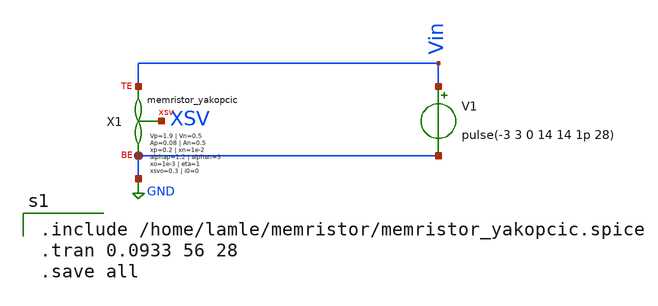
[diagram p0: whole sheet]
** sch_path: apl-paper/ngspice/test_memristor.sch
**.subckt test_memristor
V1 Vin GND pulse(-3 3 0 14 14 1p 28)
X1 GND Vin XSV memristor_yakopcic a1=23.4e-6 a2=0.4e-6 b1=1.1 b2=1.1 Vp=1.9 Vn=0.5 Ap=0.08 An=0.5
+ xp=0.2 xn=1e-2 alphap=1.2 alphan=3 xo=1e-3 eta=1 xsvo=0.3 i0=0 u1=0.72 u2=-0.76 k1=0.2 k2=5.5
**** begin user architecture code

.include /home/lamle/memristor/memristor_yakopcic.spice
.tran 0.0933 56 28
.save all

**** end user architecture code
**.ends

* expanding   symbol:  memristor/memristor_yakopcic.sym # of pins=3
** sym_path: apl-paper/ngspice/memristor_yakopcic.sym
.include /home/lamle/memristor/memristor_yakopcic.spice
.GLOBAL GND
.end
